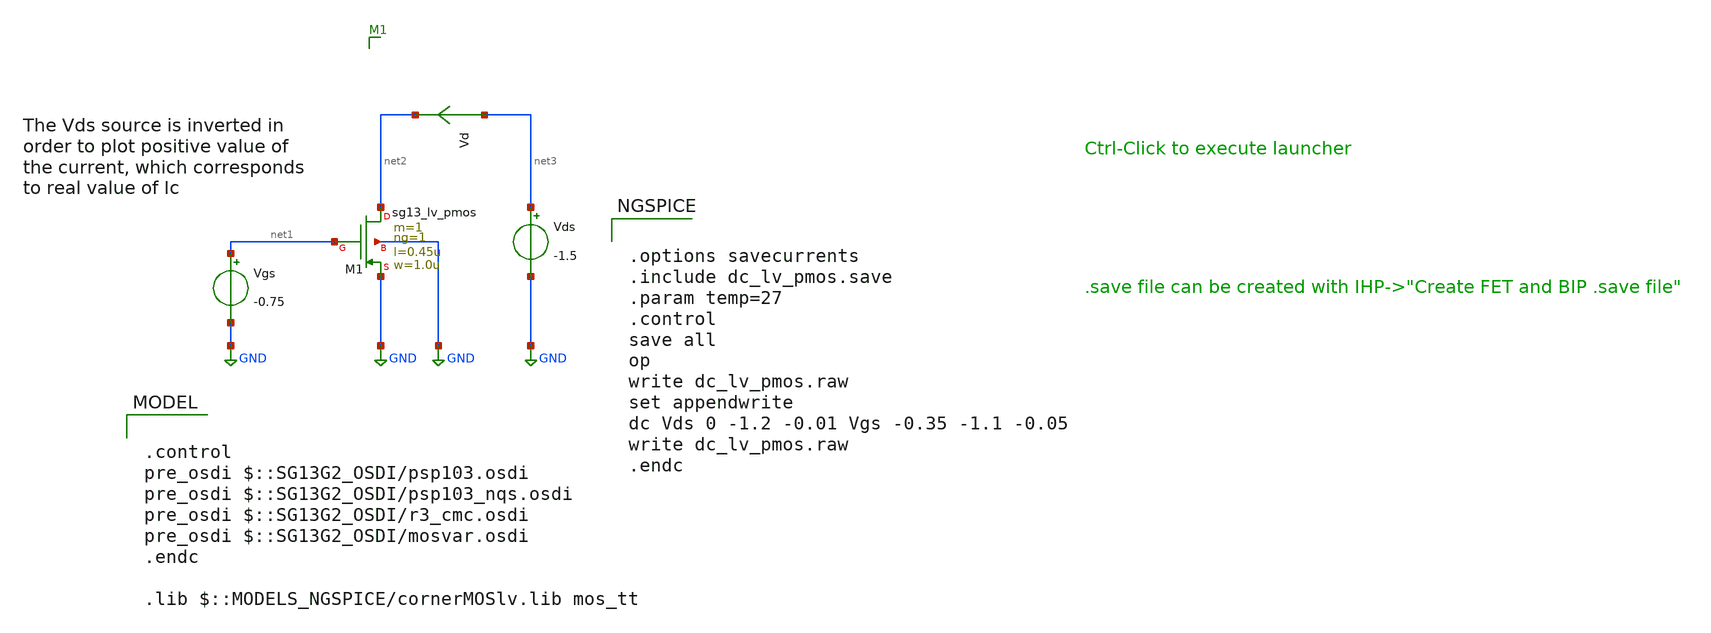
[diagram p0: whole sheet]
** sch_path: ihp-sg13g2/xschem_libs/sg13g2_tests/dc_lv_pmos/schematic/dc_lv_pmos.sch
* Copyright 2023 IHP PDK Authors
**.subckt dc_lv_pmos
Vgs net1 GND -0.75
Vds net3 GND -1.5
XM1 net2 net1 GND GND sg13_lv_pmos w=1.0u l=0.45u ng=1 m=1 mm_ok=1
Vd net3 net2 0
.save i(vd)
**** begin user architecture code

.control
pre_osdi $::SG13G2_OSDI/psp103.osdi
pre_osdi $::SG13G2_OSDI/psp103_nqs.osdi
pre_osdi $::SG13G2_OSDI/r3_cmc.osdi
pre_osdi $::SG13G2_OSDI/mosvar.osdi
.endc

.lib $::MODELS_NGSPICE/cornerMOSlv.lib mos_tt



.options savecurrents
.include dc_lv_pmos.save
.param temp=27
.control
save all
op
write dc_lv_pmos.raw
set appendwrite
dc Vds 0 -1.2 -0.01 Vgs -0.35 -1.1 -0.05
write dc_lv_pmos.raw
.endc


**** end user architecture code
**.ends
.GLOBAL GND
.end
